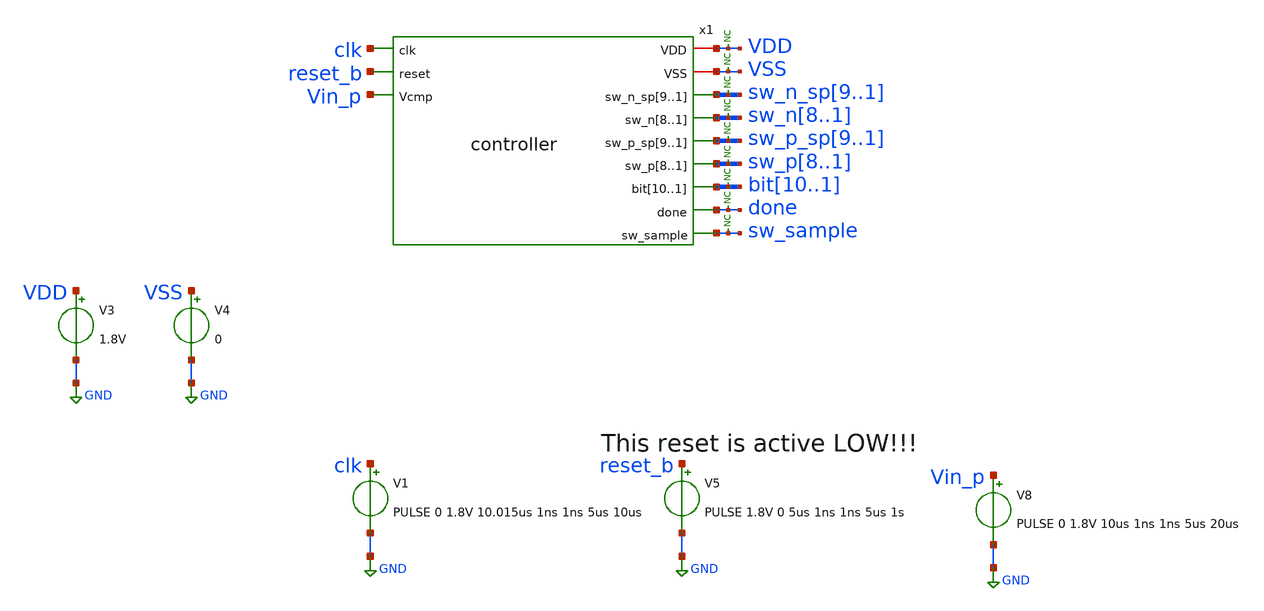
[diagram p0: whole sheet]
** sch_path: xschem/tests/controller/controller_test.sch
**.subckt controller_test
V3 VDD GND 1.8V
V4 VSS GND 0
x1 VDD VSS sw_n_sp9 sw_n_sp8 sw_n_sp7 sw_n_sp6 sw_n_sp5 sw_n_sp4 sw_n_sp3 sw_n_sp2 sw_n_sp1 clk
+ reset_b sw_n8 sw_n7 sw_n6 sw_n5 sw_n4 sw_n3 sw_n2 sw_n1 Vin_p sw_p_sp9 sw_p_sp8 sw_p_sp7 sw_p_sp6 sw_p_sp5
+ sw_p_sp4 sw_p_sp3 sw_p_sp2 sw_p_sp1 sw_p8 sw_p7 sw_p6 sw_p5 sw_p4 sw_p3 sw_p2 sw_p1 bit10 bit9 bit8 bit7
+ bit6 bit5 bit4 bit3 bit2 bit1 done sw_sample controller
V1 clk GND PULSE 0 1.8V 10.015us 1ns 1ns 5us 10us
V5 reset_b GND PULSE 1.8V 0 5us 1ns 1ns 5us 1s
V8 Vin_p GND PULSE 0 1.8V 10us 1ns 1ns 5us 20us
* noconn VDD
* noconn VSS
* noconn sw_n_sp[9..1]
* noconn sw_n[8..1]
* noconn sw_p_sp[9..1]
* noconn sw_p[8..1]
* noconn bit[10..1]
* noconn done
* noconn sw_sample
**** begin user architecture code
 .lib $::SKYWATER_MODELS/sky130.lib.spice tt
.include $::SKYWATER_STDCELLS/sky130_fd_sc_hd.spice


.options acct list
.temp 25
*vvcc VDD 0 dc 1.8
*vvss VSS 0 0
.control
tran 0.8u 400u
*plot RST_PLS clk+2 Pulse+4
plot done-4  sw_n_sp1 sw_n_sp2+2 sw_n_sp3+4 sw_n_sp4+6 sw_n_sp5+8 sw_n_sp6+10 sw_n_sp7+12
+ sw_n_sp8+14 sw_n_sp9+16 Vin_p+18 clk+20
plot done-4  sw_p_sp1 sw_p_sp2+2 sw_p_sp3+4 sw_p_sp4+6 sw_p_sp5+8 sw_p_sp6+10 sw_p_sp7+12
+ sw_p_sp8+14 sw_p_sp9+16 Vin_p+18 clk+20
plot done-4  sw_n1 sw_n2+2 sw_n3+4 sw_n4+6 sw_n5+8 sw_n6+10 sw_n7+12 sw_n8+14 Vin_p+16 clk+18
plot done-4  sw_p1 sw_p2+2 sw_p3+4 sw_p4+6 sw_p5+8 sw_p6+10 sw_p7+12 sw_p8+14 Vin_p+16 clk+18
plot done-4 bit1 bit2+2 bit3+4 bit4+6 bit5+8 bit6+10 bit7+12 bit8+14 bit9+16 bit10+18

plot done-4  sw_n_sp1 sw_n_sp2+2 sw_n_sp3+4 sw_n_sp4+6 sw_n_sp5+8 sw_n_sp6+10 sw_n_sp7+12
+ sw_n_sp8+14 sw_n_sp9+16 Vin_q+18 clk+20 sw_n1 sw_n2+2 sw_n3+4 sw_n4+6 sw_n5+8 sw_n6+10 sw_n7+12 sw_n8+14

plot done-4  sw_p_sp1 sw_p_sp2+2 sw_p_sp3+4 sw_p_sp4+6 sw_p_sp5+8 sw_p_sp6+10 sw_p_sp7+12
+ sw_p_sp8+14 sw_p_sp9+16 Vin_q+18 clk+20 sw_p1 sw_p2+2 sw_p3+4 sw_p4+6 sw_p5+8 sw_p6+10 sw_p7+12 sw_p8+14

plot clk reset_b+2 x1.cycle0+4 x1.cycle1+6 x1.cycle2+8 x1.cycle16+10 x1.cycle17+12 x1.cycle18+14
+ sw_sample+16 vin_p+18

plot reset_b-2 clk vin_p vin_n gen_clk

write controller_test.raw
.endc


**** end user architecture code
**.ends

* expanding   symbol:  src/controller/controller.sym # of pins=12
** sym_path: xschem/src/controller/controller.sym
** sch_path: xschem/src/controller/controller.sch
.subckt controller VDD VSS sw_n_sp9 sw_n_sp8 sw_n_sp7 sw_n_sp6 sw_n_sp5 sw_n_sp4 sw_n_sp3 sw_n_sp2
+ sw_n_sp1 clk reset sw_n8 sw_n7 sw_n6 sw_n5 sw_n4 sw_n3 sw_n2 sw_n1 Vcmp sw_p_sp9 sw_p_sp8 sw_p_sp7 sw_p_sp6
+ sw_p_sp5 sw_p_sp4 sw_p_sp3 sw_p_sp2 sw_p_sp1 sw_p8 sw_p7 sw_p6 sw_p5 sw_p4 sw_p3 sw_p2 sw_p1 bit10 bit9 bit8
+ bit7 bit6 bit5 bit4 bit3 bit2 bit1 done sw_sample
*.ipin clk
*.opin sw_n_sp9,sw_n_sp8,sw_n_sp7,sw_n_sp6,sw_n_sp5,sw_n_sp4,sw_n_sp3,sw_n_sp2,sw_n_sp1
*.iopin VSS
*.iopin VDD
*.ipin reset
*.ipin Vcmp
*.opin sw_n8,sw_n7,sw_n6,sw_n5,sw_n4,sw_n3,sw_n2,sw_n1
*.opin sw_p_sp9,sw_p_sp8,sw_p_sp7,sw_p_sp6,sw_p_sp5,sw_p_sp4,sw_p_sp3,sw_p_sp2,sw_p_sp1
*.opin sw_p8,sw_p7,sw_p6,sw_p5,sw_p4,sw_p3,sw_p2,sw_p1
*.opin bit10,bit9,bit8,bit7,bit6,bit5,bit4,bit3,bit2,bit1
*.opin done
*.opin sw_sample
x95 cycle1 cycle2 cycle3 cycle4 VSS VSS VDD VDD net2 sky130_fd_sc_hd__or4_2
x96 cycle5 cycle6 cycle7 cycle8 VSS VSS VDD VDD net3 sky130_fd_sc_hd__or4_2
x97 cycle9 cycle10 cycle11 cycle12 VSS VSS VDD VDD net5 sky130_fd_sc_hd__or4_2
* noconn sw_sample
x3 VDD raw_bit13 raw_bit12 raw_bit11 raw_bit10 raw_bit9 raw_bit8 raw_bit7 raw_bit6 raw_bit5 raw_bit4
+ raw_bit3 raw_bit2 raw_bit1 VSS reset bit10 bit9 bit8 bit7 bit6 bit5 bit4 bit3 bit2 bit1 done cycle31 dec
x4 raw_bit13 raw_bit12 raw_bit11 raw_bit10 raw_bit9 raw_bit8 raw_bit7 raw_bit6 raw_bit5 raw_bit4
+ raw_bit3 raw_bit2 raw_bit1 cycle30 cycle29 cycle28 cycle27 cycle26 cycle25 cycle24 cycle23 cycle22 cycle21
+ cycle20 cycle19 cycle18 sw_p8 sw_p7 sw_p6 sw_p5 sw_p4 sw_p3 sw_p2 sw_p1 Vcmp net1 VDD VSS sw_n_sp9 sw_n_sp8
+ sw_n_sp7 sw_n_sp6 sw_n_sp5 sw_n_sp4 sw_n_sp3 sw_n_sp2 sw_n_sp1 sw_n8 sw_n7 sw_n6 sw_n5 sw_n4 sw_n3 sw_n2
+ sw_n1 sw_p_sp9 sw_p_sp8 sw_p_sp7 sw_p_sp6 sw_p_sp5 sw_p_sp4 sw_p_sp3 sw_p_sp2 sw_p_sp1 raw_bit_calculator
x1 clk VDD VSS reset cycle31 cycle30 cycle29 cycle28 cycle27 cycle26 cycle25 cycle24 cycle23 cycle22
+ cycle21 cycle20 cycle19 cycle18 cycle17 cycle16 cycle15 cycle14 cycle13 cycle12 cycle11 cycle10 cycle9
+ cycle8 cycle7 cycle6 cycle5 cycle4 cycle3 cycle2 cycle1 cycle0 shifted_clock_generator
x8 net2 net3 net5 net4 VSS VSS VDD VDD net6 sky130_fd_sc_hd__or4_2
x9 clk net6 reset VSS VSS VDD VDD sw_sample sky130_fd_sc_hd__dfrtn_1
x10 cycle13 cycle14 cycle15 VSS VSS VDD VDD net4 sky130_fd_sc_hd__or3_2
x6 cycle0 VSS VSS VDD VDD net1 sky130_fd_sc_hd__inv_16
.ends


* expanding   symbol:  src/dec/dec.sym # of pins=7
** sym_path: xschem/src/dec/dec.sym
** sch_path: xschem/src/dec/dec.sch
.subckt dec VDD raw_bit13 raw_bit12 raw_bit11 raw_bit10 raw_bit9 raw_bit8 raw_bit7 raw_bit6 raw_bit5
+ raw_bit4 raw_bit3 raw_bit2 raw_bit1 VSS reset_b bit10 bit9 bit8 bit7 bit6 bit5 bit4 bit3 bit2 bit1 done
+ dump_bus
*.iopin VDD
*.iopin VSS
*.ipin reset_b
*.ipin dump_bus
*.opin done
*.ipin raw_bit13
*.ipin raw_bit12
*.ipin raw_bit11
*.ipin raw_bit10
*.ipin raw_bit9
*.ipin raw_bit8
*.ipin raw_bit7
*.ipin raw_bit6
*.ipin raw_bit5
*.ipin raw_bit4
*.ipin raw_bit3
*.ipin raw_bit2
*.ipin raw_bit1
*.opin bit10
*.opin bit9
*.opin bit8
*.opin bit7
*.opin bit6
*.opin bit5
*.opin bit4
*.opin bit3
*.opin bit2
*.opin bit1
x62 raw_bit2 raw_bit1 net1 VSS VSS VDD VDD net16 net2 sky130_fd_sc_hd__fa_1
x64 raw_bit3 raw_bit1 net4 VSS VSS VDD VDD net1 net3 sky130_fd_sc_hd__fa_1
x67 dump_bus net2 reset_b VSS VSS VDD VDD bit2 sky130_fd_sc_hd__dfrtp_1
x68 dump_bus net3 reset_b VSS VSS VDD VDD bit3 sky130_fd_sc_hd__dfrtp_1
x65 raw_bit5 raw_bit4 net5 VSS VSS VDD VDD net4 net6 sky130_fd_sc_hd__fa_1
x69 raw_bit6 raw_bit4 net8 VSS VSS VDD VDD net5 net7 sky130_fd_sc_hd__fa_1
x70 dump_bus net6 reset_b VSS VSS VDD VDD bit4 sky130_fd_sc_hd__dfrtp_1
x71 dump_bus net7 reset_b VSS VSS VDD VDD bit5 sky130_fd_sc_hd__dfrtp_1
x72 raw_bit7 raw_bit4 net9 VSS VSS VDD VDD net8 net10 sky130_fd_sc_hd__fa_1
x73 raw_bit9 raw_bit8 net12 VSS VSS VDD VDD net9 net11 sky130_fd_sc_hd__fa_1
x74 dump_bus net10 reset_b VSS VSS VDD VDD bit6 sky130_fd_sc_hd__dfrtp_1
x75 dump_bus net11 reset_b VSS VSS VDD VDD bit7 sky130_fd_sc_hd__dfrtp_1
x76 raw_bit10 raw_bit8 net13 VSS VSS VDD VDD net12 net14 sky130_fd_sc_hd__fa_1
x77 raw_bit11 raw_bit8 raw_bit12 VSS VSS VDD VDD net13 net15 sky130_fd_sc_hd__fa_1
x78 dump_bus net14 reset_b VSS VSS VDD VDD bit8 sky130_fd_sc_hd__dfrtp_1
x79 dump_bus net15 reset_b VSS VSS VDD VDD bit9 sky130_fd_sc_hd__dfrtp_1
x80 dump_bus net16 reset_b VSS VSS VDD VDD bit1 sky130_fd_sc_hd__dfrtp_1
x81 dump_bus raw_bit13 reset_b VSS VSS VDD VDD bit10 sky130_fd_sc_hd__dfrtp_1
x82 dump_bus VSS VSS VDD VDD done sky130_fd_sc_hd__inv_1
* noconn done
.ends


* expanding   symbol:  src/raw_bit_calculator/raw_bit_calculator.sym # of pins=10
** sym_path: xschem/src/raw_bit_calculator/raw_bit_calculator.sym
** sch_path: xschem/src/raw_bit_calculator/raw_bit_calculator.sch
.subckt raw_bit_calculator raw_bit13 raw_bit12 raw_bit11 raw_bit10 raw_bit9 raw_bit8 raw_bit7
+ raw_bit6 raw_bit5 raw_bit4 raw_bit3 raw_bit2 raw_bit1 cycle13 cycle12 cycle11 cycle10 cycle9 cycle8 cycle7
+ cycle6 cycle5 cycle4 cycle3 cycle2 cycle1 sw_p8 sw_p7 sw_p6 sw_p5 sw_p4 sw_p3 sw_p2 sw_p1 Vcmp RESET VDD
+ VSS sw_n_sp9 sw_n_sp8 sw_n_sp7 sw_n_sp6 sw_n_sp5 sw_n_sp4 sw_n_sp3 sw_n_sp2 sw_n_sp1 sw_n8 sw_n7 sw_n6
+ sw_n5 sw_n4 sw_n3 sw_n2 sw_n1 sw_p_sp9 sw_p_sp8 sw_p_sp7 sw_p_sp6 sw_p_sp5 sw_p_sp4 sw_p_sp3 sw_p_sp2
+ sw_p_sp1
*.ipin
*+ cycle13,cycle12,cycle11,cycle10,cycle9,cycle8,cycle7,cycle6,cycle5,cycle4,cycle3,cycle2,cycle1
*.opin sw_n_sp9,sw_n_sp8,sw_n_sp7,sw_n_sp6,sw_n_sp5,sw_n_sp4,sw_n_sp3,sw_n_sp2,sw_n_sp1
*.iopin VSS
*.iopin VDD
*.opin sw_n8,sw_n7,sw_n6,sw_n5,sw_n4,sw_n3,sw_n2,sw_n1
*.opin sw_p_sp9,sw_p_sp8,sw_p_sp7,sw_p_sp6,sw_p_sp5,sw_p_sp4,sw_p_sp3,sw_p_sp2,sw_p_sp1
*.opin sw_p8,sw_p7,sw_p6,sw_p5,sw_p4,sw_p3,sw_p2,sw_p1
*.ipin Vcmp
*.ipin RESET
*.opin
*+ raw_bit13,raw_bit12,raw_bit11,raw_bit10,raw_bit9,raw_bit8,raw_bit7,raw_bit6,raw_bit5,raw_bit4,raw_bit3,raw_bit2,raw_bit1
x29 raw_bit1 Vcmp VSS VSS VDD VDD net58 sky130_fd_sc_hd__xor2_1
x31 raw_bit1 Vcmp VSS VSS VDD VDD net62 sky130_fd_sc_hd__xor2_1
x37 raw_bit4 Vcmp VSS VSS VDD VDD net52 sky130_fd_sc_hd__xor2_1
x40 raw_bit4 Vcmp VSS VSS VDD VDD net53 sky130_fd_sc_hd__xor2_1
x45 raw_bit4 Vcmp VSS VSS VDD VDD net54 sky130_fd_sc_hd__xor2_1
x100 cycle1 net11 net23 VSS VSS VDD VDD sw_p_sp1 sky130_fd_sc_hd__dfrtp_1
x99 Vcmp VSS VSS VDD VDD net11 sky130_fd_sc_hd__inv_1
x102 cycle1 Vcmp net23 VSS VSS VDD VDD sw_n_sp1 sky130_fd_sc_hd__dfrtp_1
x25 cycle1 Vcmp net25 VSS VSS VDD VDD sw_n_sp2 sky130_fd_sc_hd__dfrtp_1
x103 Vcmp VSS VSS VDD VDD net12 sky130_fd_sc_hd__inv_1
x104 cycle1 net12 net25 VSS VSS VDD VDD sw_p_sp2 sky130_fd_sc_hd__dfrtp_1
x21 net1 Vcmp RESET VSS VSS VDD VDD sw_n1 sky130_fd_sc_hd__dfstp_1
x22 net1 net13 RESET VSS VSS VDD VDD sw_p1 sky130_fd_sc_hd__dfstp_1
x105 Vcmp VSS VSS VDD VDD net13 sky130_fd_sc_hd__inv_1
x28 net4 Vcmp RESET VSS VSS VDD VDD sw_n2 sky130_fd_sc_hd__dfstp_1
x106 net4 net14 RESET VSS VSS VDD VDD sw_p2 sky130_fd_sc_hd__dfstp_1
x107 Vcmp VSS VSS VDD VDD net14 sky130_fd_sc_hd__inv_1
x109 Vcmp VSS VSS VDD VDD net15 sky130_fd_sc_hd__inv_1
x111 Vcmp VSS VSS VDD VDD net16 sky130_fd_sc_hd__inv_1
x27 cycle4 Vcmp net27 VSS VSS VDD VDD sw_n_sp3 sky130_fd_sc_hd__dfrtp_1
x35 cycle4 net15 net27 VSS VSS VDD VDD sw_p_sp3 sky130_fd_sc_hd__dfrtp_1
x41 cycle4 Vcmp net28 VSS VSS VDD VDD sw_n_sp4 sky130_fd_sc_hd__dfrtp_1
x108 cycle4 net16 net28 VSS VSS VDD VDD sw_p_sp4 sky130_fd_sc_hd__dfrtp_1
x110 cycle4 Vcmp net29 VSS VSS VDD VDD sw_n_sp5 sky130_fd_sc_hd__dfrtp_1
x112 cycle4 net17 net29 VSS VSS VDD VDD sw_p_sp5 sky130_fd_sc_hd__dfrtp_1
x113 Vcmp VSS VSS VDD VDD net17 sky130_fd_sc_hd__inv_1
x114 net6 net18 RESET VSS VSS VDD VDD sw_p3 sky130_fd_sc_hd__dfstp_1
x32 net6 Vcmp RESET VSS VSS VDD VDD sw_n3 sky130_fd_sc_hd__dfstp_1
x115 Vcmp VSS VSS VDD VDD net18 sky130_fd_sc_hd__inv_1
x38 net7 Vcmp RESET VSS VSS VDD VDD sw_n4 sky130_fd_sc_hd__dfstp_1
x116 net7 net19 RESET VSS VSS VDD VDD sw_p4 sky130_fd_sc_hd__dfstp_1
x117 Vcmp VSS VSS VDD VDD net19 sky130_fd_sc_hd__inv_1
x43 net8 Vcmp RESET VSS VSS VDD VDD sw_n5 sky130_fd_sc_hd__dfstp_1
x118 net8 net20 RESET VSS VSS VDD VDD sw_p5 sky130_fd_sc_hd__dfstp_1
x119 Vcmp VSS VSS VDD VDD net20 sky130_fd_sc_hd__inv_1
x132 cycle12 net21 RESET VSS VSS VDD VDD sw_p_sp9 sky130_fd_sc_hd__dfrtp_1
x133 Vcmp VSS VSS VDD VDD net21 sky130_fd_sc_hd__inv_1
x61 cycle12 Vcmp RESET VSS VSS VDD VDD sw_n_sp9 sky130_fd_sc_hd__dfrtp_1
x24 net51 VDD VSS net1 net3 net2 demux2
x30 net61 VDD VSS net4 net60 net5 demux2
x34 net65 VDD VSS net6 net64 net22 demux2
x39 net68 VDD VSS net7 net67 net9 demux2
x44 net71 VDD VSS net8 net70 net10 demux2
x1 net2 VSS VSS VDD VDD net24 sky130_fd_sc_hd__inv_1
x2 net5 VSS VSS VDD VDD net26 sky130_fd_sc_hd__inv_1
x3 cycle1 Vcmp RESET VSS VSS VDD VDD raw_bit1 sky130_fd_sc_hd__dfrtp_4
x4 cycle2 Vcmp RESET VSS VSS VDD VDD raw_bit2 sky130_fd_sc_hd__dfrtp_4
x5 cycle3 Vcmp RESET VSS VSS VDD VDD raw_bit3 sky130_fd_sc_hd__dfrtp_4
x6 cycle4 Vcmp RESET VSS VSS VDD VDD raw_bit4 sky130_fd_sc_hd__dfrtp_4
x7 cycle5 Vcmp RESET VSS VSS VDD VDD raw_bit5 sky130_fd_sc_hd__dfrtp_4
x8 cycle6 Vcmp RESET VSS VSS VDD VDD raw_bit6 sky130_fd_sc_hd__dfrtp_4
x9 cycle7 Vcmp RESET VSS VSS VDD VDD raw_bit7 sky130_fd_sc_hd__dfrtp_4
x10 cycle8 Vcmp RESET VSS VSS VDD VDD raw_bit8 sky130_fd_sc_hd__dfrtp_4
x11 cycle9 Vcmp RESET VSS VSS VDD VDD raw_bit9 sky130_fd_sc_hd__dfrtp_4
x12 cycle10 Vcmp RESET VSS VSS VDD VDD raw_bit10 sky130_fd_sc_hd__dfrtp_4
x13 cycle11 Vcmp RESET VSS VSS VDD VDD raw_bit11 sky130_fd_sc_hd__dfrtp_4
x14 cycle12 Vcmp RESET VSS VSS VDD VDD raw_bit12 sky130_fd_sc_hd__dfrtp_4
x15 cycle13 Vcmp RESET VSS VSS VDD VDD raw_bit13 sky130_fd_sc_hd__dfrtp_4
x18 net22 VSS VSS VDD VDD net30 sky130_fd_sc_hd__inv_1
x19 net9 VSS VSS VDD VDD net31 sky130_fd_sc_hd__inv_1
x20 net10 VSS VSS VDD VDD net32 sky130_fd_sc_hd__inv_1
x42 raw_bit8 Vcmp VSS VSS VDD VDD net55 sky130_fd_sc_hd__xor2_1
x62 raw_bit8 Vcmp VSS VSS VDD VDD net56 sky130_fd_sc_hd__xor2_1
x64 raw_bit8 Vcmp VSS VSS VDD VDD net57 sky130_fd_sc_hd__xor2_1
x65 Vcmp VSS VSS VDD VDD net38 sky130_fd_sc_hd__inv_1
x66 Vcmp VSS VSS VDD VDD net39 sky130_fd_sc_hd__inv_1
x67 cycle8 Vcmp net45 VSS VSS VDD VDD sw_n_sp6 sky130_fd_sc_hd__dfrtp_1
x68 cycle8 net38 net45 VSS VSS VDD VDD sw_p_sp6 sky130_fd_sc_hd__dfrtp_1
x69 cycle8 Vcmp net46 VSS VSS VDD VDD sw_n_sp7 sky130_fd_sc_hd__dfrtp_1
x70 cycle8 net39 net46 VSS VSS VDD VDD sw_p_sp7 sky130_fd_sc_hd__dfrtp_1
x71 cycle8 Vcmp net47 VSS VSS VDD VDD sw_n_sp8 sky130_fd_sc_hd__dfrtp_1
x72 cycle8 net40 net47 VSS VSS VDD VDD sw_p_sp8 sky130_fd_sc_hd__dfrtp_1
x73 Vcmp VSS VSS VDD VDD net40 sky130_fd_sc_hd__inv_1
x74 net33 net41 RESET VSS VSS VDD VDD sw_p6 sky130_fd_sc_hd__dfstp_1
x75 net33 Vcmp RESET VSS VSS VDD VDD sw_n6 sky130_fd_sc_hd__dfstp_1
x76 Vcmp VSS VSS VDD VDD net41 sky130_fd_sc_hd__inv_1
x77 net34 Vcmp RESET VSS VSS VDD VDD sw_n7 sky130_fd_sc_hd__dfstp_1
x78 net34 net42 RESET VSS VSS VDD VDD sw_p7 sky130_fd_sc_hd__dfstp_1
x79 Vcmp VSS VSS VDD VDD net42 sky130_fd_sc_hd__inv_1
x80 net35 Vcmp RESET VSS VSS VDD VDD sw_n8 sky130_fd_sc_hd__dfstp_1
x81 net35 net43 RESET VSS VSS VDD VDD sw_p8 sky130_fd_sc_hd__dfstp_1
x82 Vcmp VSS VSS VDD VDD net43 sky130_fd_sc_hd__inv_1
x83 net74 VDD VSS net33 net73 net44 demux2
x84 net77 VDD VSS net34 net76 net36 demux2
x85 net80 VDD VSS net35 net79 net37 demux2
x88 net44 VSS VSS VDD VDD net48 sky130_fd_sc_hd__inv_1
x89 net36 VSS VSS VDD VDD net49 sky130_fd_sc_hd__inv_1
x90 net37 VSS VSS VDD VDD net50 sky130_fd_sc_hd__inv_1
x46 net24 RESET VSS VSS VDD VDD net23 sky130_fd_sc_hd__and2_0
x23 net26 RESET VSS VSS VDD VDD net25 sky130_fd_sc_hd__and2_0
x26 net30 RESET VSS VSS VDD VDD net27 sky130_fd_sc_hd__and2_0
x16 net31 RESET VSS VSS VDD VDD net28 sky130_fd_sc_hd__and2_0
x17 net32 RESET VSS VSS VDD VDD net29 sky130_fd_sc_hd__and2_0
x33 net48 RESET VSS VSS VDD VDD net45 sky130_fd_sc_hd__and2_0
x36 net49 RESET VSS VSS VDD VDD net46 sky130_fd_sc_hd__and2_0
x47 net50 RESET VSS VSS VDD VDD net47 sky130_fd_sc_hd__and2_0
x48 cycle2 net58 RESET VSS VSS VDD VDD net51 sky130_fd_sc_hd__dfrtp_1
x49 net59 VSS VSS VDD VDD net3 sky130_fd_sc_hd__clkdlybuf4s50_1
x50 cycle2 VSS VSS VDD VDD net59 sky130_fd_sc_hd__clkdlybuf4s50_1
x51 cycle3 net62 RESET VSS VSS VDD VDD net61 sky130_fd_sc_hd__dfrtp_1
x52 net63 VSS VSS VDD VDD net60 sky130_fd_sc_hd__clkdlybuf4s50_1
x53 cycle3 VSS VSS VDD VDD net63 sky130_fd_sc_hd__clkdlybuf4s50_1
x54 cycle5 net52 RESET VSS VSS VDD VDD net65 sky130_fd_sc_hd__dfrtp_1
x55 net66 VSS VSS VDD VDD net64 sky130_fd_sc_hd__clkdlybuf4s50_1
x56 cycle5 VSS VSS VDD VDD net66 sky130_fd_sc_hd__clkdlybuf4s50_1
x57 cycle6 net53 RESET VSS VSS VDD VDD net68 sky130_fd_sc_hd__dfrtp_1
x58 net69 VSS VSS VDD VDD net67 sky130_fd_sc_hd__clkdlybuf4s50_1
x59 cycle6 VSS VSS VDD VDD net69 sky130_fd_sc_hd__clkdlybuf4s50_1
x60 cycle7 net54 RESET VSS VSS VDD VDD net71 sky130_fd_sc_hd__dfrtp_1
x63 net72 VSS VSS VDD VDD net70 sky130_fd_sc_hd__clkdlybuf4s50_1
x86 cycle7 VSS VSS VDD VDD net72 sky130_fd_sc_hd__clkdlybuf4s50_1
x87 cycle9 net55 RESET VSS VSS VDD VDD net74 sky130_fd_sc_hd__dfrtp_1
x91 net75 VSS VSS VDD VDD net73 sky130_fd_sc_hd__clkdlybuf4s50_1
x92 cycle9 VSS VSS VDD VDD net75 sky130_fd_sc_hd__clkdlybuf4s50_1
x93 cycle10 net56 RESET VSS VSS VDD VDD net77 sky130_fd_sc_hd__dfrtp_1
x94 net78 VSS VSS VDD VDD net76 sky130_fd_sc_hd__clkdlybuf4s50_1
x95 cycle10 VSS VSS VDD VDD net78 sky130_fd_sc_hd__clkdlybuf4s50_1
x96 cycle11 net57 RESET VSS VSS VDD VDD net80 sky130_fd_sc_hd__dfrtp_1
x97 net81 VSS VSS VDD VDD net79 sky130_fd_sc_hd__clkdlybuf4s50_1
x98 cycle11 VSS VSS VDD VDD net81 sky130_fd_sc_hd__clkdlybuf4s50_1
.ends


* expanding   symbol:  src/shifted_clock_generator/shifted_clock_generator.sym # of pins=5
** sym_path: xschem/src/shifted_clock_generator/shifted_clock_generator.sym
** sch_path: xschem/src/shifted_clock_generator/shifted_clock_generator.sch
.subckt shifted_clock_generator clk VDD VSS reset cycle31 cycle30 cycle29 cycle28 cycle27 cycle26
+ cycle25 cycle24 cycle23 cycle22 cycle21 cycle20 cycle19 cycle18 cycle17 cycle16 cycle15 cycle14 cycle13
+ cycle12 cycle11 cycle10 cycle9 cycle8 cycle7 cycle6 cycle5 cycle4 cycle3 cycle2 cycle1 cycle0
*.opin
*+ cycle31,cycle30,cycle29,cycle28,cycle27,cycle26,cycle25,cycle24,cycle23,cycle22,cycle21,cycle20,cycle19,cycle18,cycle17,cycle16,cycle15,cycle14,cycle13,cycle12,cycle11,cycle10,cycle9,cycle8,cycle7,cycle6,cycle5,cycle4,cycle3,cycle2,cycle1,cycle0
*.iopin VSS
*.iopin VDD
*.ipin clk
*.ipin reset
x32 clk cycle0 reset_b VSS VSS VDD VDD cycle1 sky130_fd_sc_hd__dfrtp_1
x1 clk cycle1 reset_b VSS VSS VDD VDD cycle2 sky130_fd_sc_hd__dfrtp_1
x2 clk cycle2 reset_b VSS VSS VDD VDD cycle3 sky130_fd_sc_hd__dfrtp_1
x3 clk cycle3 reset_b VSS VSS VDD VDD cycle4 sky130_fd_sc_hd__dfrtp_1
x4 clk cycle4 reset_b VSS VSS VDD VDD cycle5 sky130_fd_sc_hd__dfrtp_1
x5 clk cycle5 reset_b VSS VSS VDD VDD cycle6 sky130_fd_sc_hd__dfrtp_1
x6 clk cycle6 reset_b VSS VSS VDD VDD cycle7 sky130_fd_sc_hd__dfrtp_1
x7 clk cycle7 reset_b VSS VSS VDD VDD cycle8 sky130_fd_sc_hd__dfrtp_1
x8 clk cycle8 reset_b VSS VSS VDD VDD cycle9 sky130_fd_sc_hd__dfrtp_1
x9 clk cycle9 reset_b VSS VSS VDD VDD cycle10 sky130_fd_sc_hd__dfrtp_1
x10 clk cycle10 reset_b VSS VSS VDD VDD cycle11 sky130_fd_sc_hd__dfrtp_1
x11 clk cycle11 reset_b VSS VSS VDD VDD cycle12 sky130_fd_sc_hd__dfrtp_1
x12 clk cycle12 reset_b VSS VSS VDD VDD cycle13 sky130_fd_sc_hd__dfrtp_1
x13 clk cycle13 reset_b VSS VSS VDD VDD cycle14 sky130_fd_sc_hd__dfrtp_1
x14 clk cycle14 reset_b VSS VSS VDD VDD cycle15 sky130_fd_sc_hd__dfrtp_1
x15 clk cycle15 reset_b VSS VSS VDD VDD cycle16 sky130_fd_sc_hd__dfrtp_1
x16 clk cycle16 reset_b VSS VSS VDD VDD cycle17 sky130_fd_sc_hd__dfrtp_1
x17 clk cycle17 reset_b VSS VSS VDD VDD cycle18 sky130_fd_sc_hd__dfrtp_1
x18 clk cycle18 reset_b VSS VSS VDD VDD cycle19 sky130_fd_sc_hd__dfrtp_1
x19 clk cycle19 reset_b VSS VSS VDD VDD cycle20 sky130_fd_sc_hd__dfrtp_1
x20 clk cycle20 reset_b VSS VSS VDD VDD cycle21 sky130_fd_sc_hd__dfrtp_1
x21 clk cycle21 reset_b VSS VSS VDD VDD cycle22 sky130_fd_sc_hd__dfrtp_1
x22 clk cycle22 reset_b VSS VSS VDD VDD cycle23 sky130_fd_sc_hd__dfrtp_1
x23 clk cycle23 reset_b VSS VSS VDD VDD cycle24 sky130_fd_sc_hd__dfrtp_1
x24 clk cycle24 reset_b VSS VSS VDD VDD cycle25 sky130_fd_sc_hd__dfrtp_1
x25 clk cycle25 reset_b VSS VSS VDD VDD cycle26 sky130_fd_sc_hd__dfrtp_1
x26 clk cycle26 reset_b VSS VSS VDD VDD cycle27 sky130_fd_sc_hd__dfrtp_1
x27 clk cycle27 reset_b VSS VSS VDD VDD cycle28 sky130_fd_sc_hd__dfrtp_1
x28 clk cycle28 reset_b VSS VSS VDD VDD cycle29 sky130_fd_sc_hd__dfrtp_1
x29 clk cycle29 reset_b VSS VSS VDD VDD cycle30 sky130_fd_sc_hd__dfrtp_1
x30 clk cycle30 reset_b VSS VSS VDD VDD cycle31 sky130_fd_sc_hd__dfrtp_1
x31 clk VDD reset_b VSS VSS VDD VDD cycle0 sky130_fd_sc_hd__dfrtp_1
x37 net1 VSS VSS VDD VDD reset_b sky130_fd_sc_hd__buf_16
x35 reset_cycle reset VSS VSS VDD VDD net1 sky130_fd_sc_hd__and2_4
x34 net5 VSS VSS VDD VDD net6 sky130_fd_sc_hd__clkdlybuf4s50_1
x39 half_cycle net12 VSS VSS VDD VDD reset_cycle sky130_fd_sc_hd__xnor2_1
x36 net4 VSS VSS VDD VDD net5 sky130_fd_sc_hd__clkdlybuf4s50_1
x40 net3 VSS VSS VDD VDD net4 sky130_fd_sc_hd__clkdlybuf4s50_1
x41 net2 VSS VSS VDD VDD net3 sky130_fd_sc_hd__clkdlybuf4s50_1
x42 half_cycle VSS VSS VDD VDD net2 sky130_fd_sc_hd__clkdlybuf4s50_1
x33 net7 cycle31 reset_b VSS VSS VDD VDD half_cycle sky130_fd_sc_hd__dfrtn_1
x38 net11 VSS VSS VDD VDD net12 sky130_fd_sc_hd__clkdlybuf4s50_1
x43 net10 VSS VSS VDD VDD net11 sky130_fd_sc_hd__clkdlybuf4s50_1
x44 net9 VSS VSS VDD VDD net10 sky130_fd_sc_hd__clkdlybuf4s50_1
x45 net8 VSS VSS VDD VDD net9 sky130_fd_sc_hd__clkdlybuf4s50_1
x46 net6 VSS VSS VDD VDD net8 sky130_fd_sc_hd__clkdlybuf4s50_1
x47 clk VSS VSS VDD VDD net7 sky130_fd_sc_hd__buf_1
.ends


* expanding   symbol:  src/demux2/demux2.sym # of pins=6
** sym_path: xschem/src/demux2/demux2.sym
** sch_path: xschem/src/demux2/demux2.sch
.subckt demux2 S VDD VSS OUT_0 IN OUT_1
*.ipin S
*.opin OUT_0
*.ipin IN
*.opin OUT_1
*.iopin VDD
*.iopin VSS
x1 net1 IN VSS VSS VDD VDD OUT_0 sky130_fd_sc_hd__and2_0
x2 S IN VSS VSS VDD VDD OUT_1 sky130_fd_sc_hd__and2_0
x3 S VSS VSS VDD VDD net1 sky130_fd_sc_hd__inv_1
.ends

.GLOBAL GND
.end
